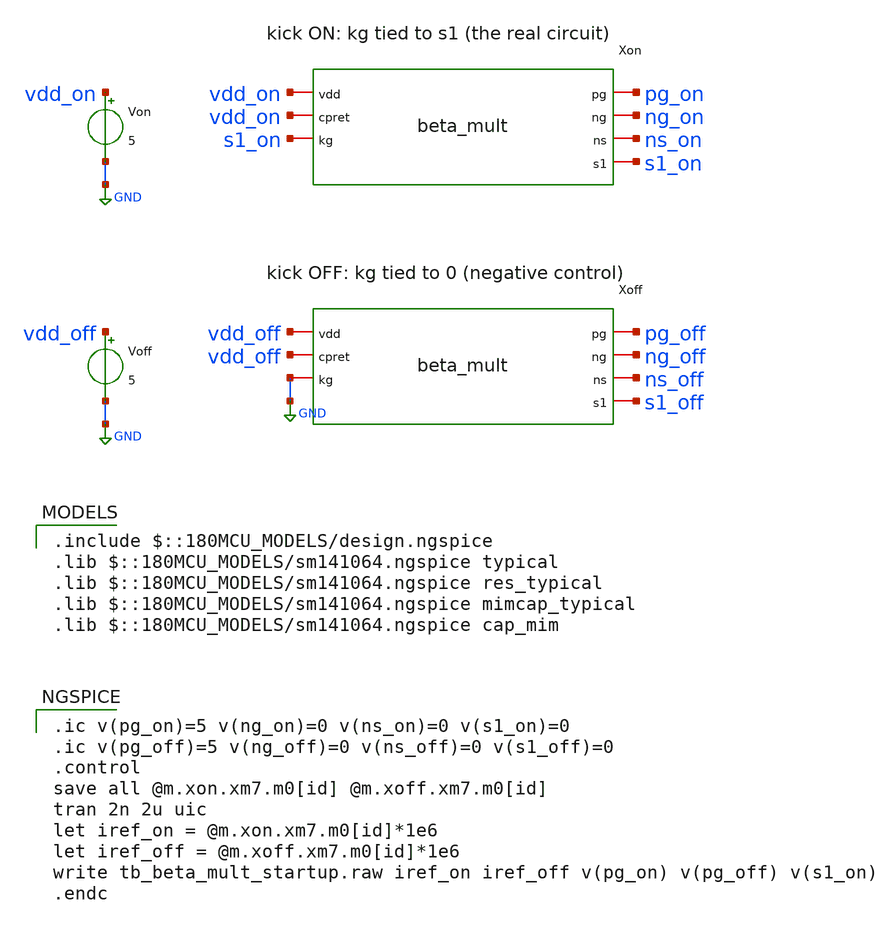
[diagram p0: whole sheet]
** sch_path: schematic pt2/sims/tb/tb_beta_mult_startup.sch
**.subckt tb_beta_mult_startup
Von vdd_on GND 5
Voff vdd_off GND 5
Xon vdd_on pg_on ng_on ns_on vdd_on s1_on s1_on beta_mult
Xoff vdd_off pg_off ng_off ns_off vdd_off s1_off GND beta_mult
**** begin user architecture code
 .include $::180MCU_MODELS/design.ngspice
.lib $::180MCU_MODELS/sm141064.ngspice typical
.lib $::180MCU_MODELS/sm141064.ngspice res_typical
.lib $::180MCU_MODELS/sm141064.ngspice mimcap_typical
.lib $::180MCU_MODELS/sm141064.ngspice cap_mim

.ic v(pg_on)=5 v(ng_on)=0 v(ns_on)=0 v(s1_on)=0
.ic v(pg_off)=5 v(ng_off)=0 v(ns_off)=0 v(s1_off)=0
.control
save all @m.xon.xm7.m0[id] @m.xoff.xm7.m0[id]
tran 2n 2u uic
let iref_on = @m.xon.xm7.m0[id]*1e6
let iref_off = @m.xoff.xm7.m0[id]*1e6
write tb_beta_mult_startup.raw iref_on iref_off v(pg_on) v(pg_off) v(s1_on)
.endc

**** end user architecture code
**.ends
.GLOBAL GND
.end
